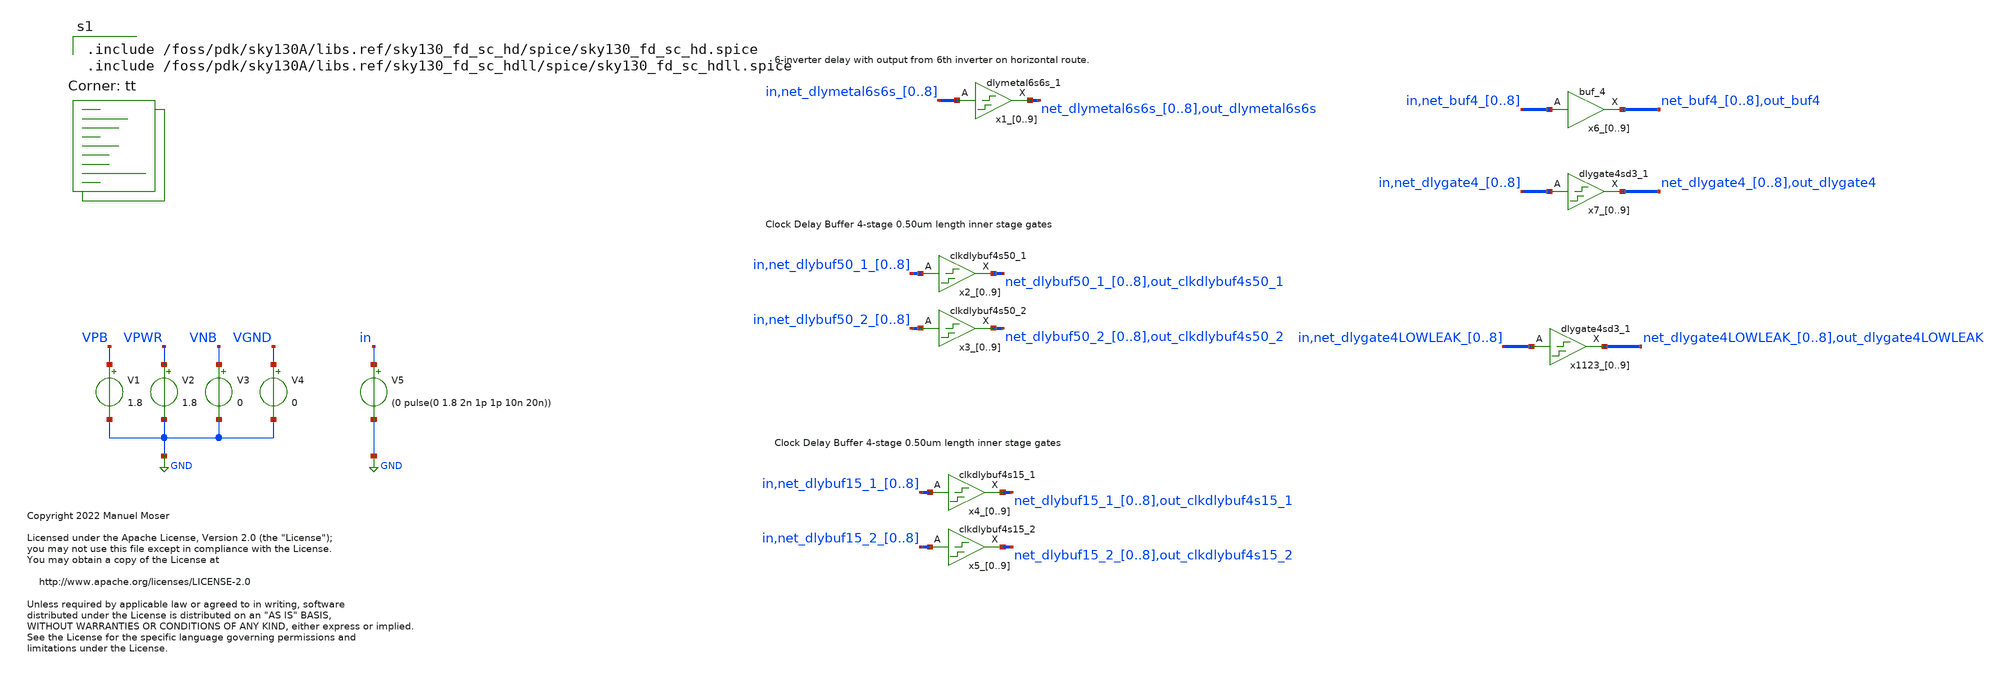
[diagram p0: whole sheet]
** sch_path: xschem/archive/adc_edge_detect_delay/delay_tb.sch
* Copyright 2022 Manuel Moser
* Licensed under the Apache License, Version 2.0 (the "License");
**.subckt delay_tb
x1_0 in VGND VNB VPB VPWR net_dlymetal6s6s_0 sky130_fd_sc_hd__dlymetal6s6s_1
x1_1 net_dlymetal6s6s_0 VGND VNB VPB VPWR net_dlymetal6s6s_1 sky130_fd_sc_hd__dlymetal6s6s_1
x1_2 net_dlymetal6s6s_1 VGND VNB VPB VPWR net_dlymetal6s6s_2 sky130_fd_sc_hd__dlymetal6s6s_1
x1_3 net_dlymetal6s6s_2 VGND VNB VPB VPWR net_dlymetal6s6s_3 sky130_fd_sc_hd__dlymetal6s6s_1
x1_4 net_dlymetal6s6s_3 VGND VNB VPB VPWR net_dlymetal6s6s_4 sky130_fd_sc_hd__dlymetal6s6s_1
x1_5 net_dlymetal6s6s_4 VGND VNB VPB VPWR net_dlymetal6s6s_5 sky130_fd_sc_hd__dlymetal6s6s_1
x1_6 net_dlymetal6s6s_5 VGND VNB VPB VPWR net_dlymetal6s6s_6 sky130_fd_sc_hd__dlymetal6s6s_1
x1_7 net_dlymetal6s6s_6 VGND VNB VPB VPWR net_dlymetal6s6s_7 sky130_fd_sc_hd__dlymetal6s6s_1
x1_8 net_dlymetal6s6s_7 VGND VNB VPB VPWR net_dlymetal6s6s_8 sky130_fd_sc_hd__dlymetal6s6s_1
x1_9 net_dlymetal6s6s_8 VGND VNB VPB VPWR out_dlymetal6s6s sky130_fd_sc_hd__dlymetal6s6s_1
x3_0 in VGND VNB VPB VPWR net_dlybuf50_2_0 sky130_fd_sc_hd__clkdlybuf4s50_2
x3_1 net_dlybuf50_2_0 VGND VNB VPB VPWR net_dlybuf50_2_1 sky130_fd_sc_hd__clkdlybuf4s50_2
x3_2 net_dlybuf50_2_1 VGND VNB VPB VPWR net_dlybuf50_2_2 sky130_fd_sc_hd__clkdlybuf4s50_2
x3_3 net_dlybuf50_2_2 VGND VNB VPB VPWR net_dlybuf50_2_3 sky130_fd_sc_hd__clkdlybuf4s50_2
x3_4 net_dlybuf50_2_3 VGND VNB VPB VPWR net_dlybuf50_2_4 sky130_fd_sc_hd__clkdlybuf4s50_2
x3_5 net_dlybuf50_2_4 VGND VNB VPB VPWR net_dlybuf50_2_5 sky130_fd_sc_hd__clkdlybuf4s50_2
x3_6 net_dlybuf50_2_5 VGND VNB VPB VPWR net_dlybuf50_2_6 sky130_fd_sc_hd__clkdlybuf4s50_2
x3_7 net_dlybuf50_2_6 VGND VNB VPB VPWR net_dlybuf50_2_7 sky130_fd_sc_hd__clkdlybuf4s50_2
x3_8 net_dlybuf50_2_7 VGND VNB VPB VPWR net_dlybuf50_2_8 sky130_fd_sc_hd__clkdlybuf4s50_2
x3_9 net_dlybuf50_2_8 VGND VNB VPB VPWR out_clkdlybuf4s50_2 sky130_fd_sc_hd__clkdlybuf4s50_2
x2_0 in VGND VNB VPB VPWR net_dlybuf50_1_0 sky130_fd_sc_hd__clkdlybuf4s50_1
x2_1 net_dlybuf50_1_0 VGND VNB VPB VPWR net_dlybuf50_1_1 sky130_fd_sc_hd__clkdlybuf4s50_1
x2_2 net_dlybuf50_1_1 VGND VNB VPB VPWR net_dlybuf50_1_2 sky130_fd_sc_hd__clkdlybuf4s50_1
x2_3 net_dlybuf50_1_2 VGND VNB VPB VPWR net_dlybuf50_1_3 sky130_fd_sc_hd__clkdlybuf4s50_1
x2_4 net_dlybuf50_1_3 VGND VNB VPB VPWR net_dlybuf50_1_4 sky130_fd_sc_hd__clkdlybuf4s50_1
x2_5 net_dlybuf50_1_4 VGND VNB VPB VPWR net_dlybuf50_1_5 sky130_fd_sc_hd__clkdlybuf4s50_1
x2_6 net_dlybuf50_1_5 VGND VNB VPB VPWR net_dlybuf50_1_6 sky130_fd_sc_hd__clkdlybuf4s50_1
x2_7 net_dlybuf50_1_6 VGND VNB VPB VPWR net_dlybuf50_1_7 sky130_fd_sc_hd__clkdlybuf4s50_1
x2_8 net_dlybuf50_1_7 VGND VNB VPB VPWR net_dlybuf50_1_8 sky130_fd_sc_hd__clkdlybuf4s50_1
x2_9 net_dlybuf50_1_8 VGND VNB VPB VPWR out_clkdlybuf4s50_1 sky130_fd_sc_hd__clkdlybuf4s50_1
V1 VPB GND 1.8
V2 VPWR GND 1.8
V3 VNB GND 0
V4 VGND GND 0
V5 in GND (0 pulse(0 1.8 2n 1p 1p 10n 20n))
x5_0 in VGND VNB VPB VPWR net_dlybuf15_2_0 sky130_fd_sc_hd__clkdlybuf4s15_2
x5_1 net_dlybuf15_2_0 VGND VNB VPB VPWR net_dlybuf15_2_1 sky130_fd_sc_hd__clkdlybuf4s15_2
x5_2 net_dlybuf15_2_1 VGND VNB VPB VPWR net_dlybuf15_2_2 sky130_fd_sc_hd__clkdlybuf4s15_2
x5_3 net_dlybuf15_2_2 VGND VNB VPB VPWR net_dlybuf15_2_3 sky130_fd_sc_hd__clkdlybuf4s15_2
x5_4 net_dlybuf15_2_3 VGND VNB VPB VPWR net_dlybuf15_2_4 sky130_fd_sc_hd__clkdlybuf4s15_2
x5_5 net_dlybuf15_2_4 VGND VNB VPB VPWR net_dlybuf15_2_5 sky130_fd_sc_hd__clkdlybuf4s15_2
x5_6 net_dlybuf15_2_5 VGND VNB VPB VPWR net_dlybuf15_2_6 sky130_fd_sc_hd__clkdlybuf4s15_2
x5_7 net_dlybuf15_2_6 VGND VNB VPB VPWR net_dlybuf15_2_7 sky130_fd_sc_hd__clkdlybuf4s15_2
x5_8 net_dlybuf15_2_7 VGND VNB VPB VPWR net_dlybuf15_2_8 sky130_fd_sc_hd__clkdlybuf4s15_2
x5_9 net_dlybuf15_2_8 VGND VNB VPB VPWR out_clkdlybuf4s15_2 sky130_fd_sc_hd__clkdlybuf4s15_2
x4_0 in VGND VNB VPB VPWR net_dlybuf15_1_0 sky130_fd_sc_hd__clkdlybuf4s15_1
x4_1 net_dlybuf15_1_0 VGND VNB VPB VPWR net_dlybuf15_1_1 sky130_fd_sc_hd__clkdlybuf4s15_1
x4_2 net_dlybuf15_1_1 VGND VNB VPB VPWR net_dlybuf15_1_2 sky130_fd_sc_hd__clkdlybuf4s15_1
x4_3 net_dlybuf15_1_2 VGND VNB VPB VPWR net_dlybuf15_1_3 sky130_fd_sc_hd__clkdlybuf4s15_1
x4_4 net_dlybuf15_1_3 VGND VNB VPB VPWR net_dlybuf15_1_4 sky130_fd_sc_hd__clkdlybuf4s15_1
x4_5 net_dlybuf15_1_4 VGND VNB VPB VPWR net_dlybuf15_1_5 sky130_fd_sc_hd__clkdlybuf4s15_1
x4_6 net_dlybuf15_1_5 VGND VNB VPB VPWR net_dlybuf15_1_6 sky130_fd_sc_hd__clkdlybuf4s15_1
x4_7 net_dlybuf15_1_6 VGND VNB VPB VPWR net_dlybuf15_1_7 sky130_fd_sc_hd__clkdlybuf4s15_1
x4_8 net_dlybuf15_1_7 VGND VNB VPB VPWR net_dlybuf15_1_8 sky130_fd_sc_hd__clkdlybuf4s15_1
x4_9 net_dlybuf15_1_8 VGND VNB VPB VPWR out_clkdlybuf4s15_1 sky130_fd_sc_hd__clkdlybuf4s15_1
x6_0 in VGND VNB VPB VPWR net_buf4_0 sky130_fd_sc_hd__buf_4
x6_1 net_buf4_0 VGND VNB VPB VPWR net_buf4_1 sky130_fd_sc_hd__buf_4
x6_2 net_buf4_1 VGND VNB VPB VPWR net_buf4_2 sky130_fd_sc_hd__buf_4
x6_3 net_buf4_2 VGND VNB VPB VPWR net_buf4_3 sky130_fd_sc_hd__buf_4
x6_4 net_buf4_3 VGND VNB VPB VPWR net_buf4_4 sky130_fd_sc_hd__buf_4
x6_5 net_buf4_4 VGND VNB VPB VPWR net_buf4_5 sky130_fd_sc_hd__buf_4
x6_6 net_buf4_5 VGND VNB VPB VPWR net_buf4_6 sky130_fd_sc_hd__buf_4
x6_7 net_buf4_6 VGND VNB VPB VPWR net_buf4_7 sky130_fd_sc_hd__buf_4
x6_8 net_buf4_7 VGND VNB VPB VPWR net_buf4_8 sky130_fd_sc_hd__buf_4
x6_9 net_buf4_8 VGND VNB VPB VPWR out_buf4 sky130_fd_sc_hd__buf_4
x7_0 in VGND VNB VPB VPWR net_dlygate4_0 sky130_fd_sc_hd__dlygate4sd3_1
x7_1 net_dlygate4_0 VGND VNB VPB VPWR net_dlygate4_1 sky130_fd_sc_hd__dlygate4sd3_1
x7_2 net_dlygate4_1 VGND VNB VPB VPWR net_dlygate4_2 sky130_fd_sc_hd__dlygate4sd3_1
x7_3 net_dlygate4_2 VGND VNB VPB VPWR net_dlygate4_3 sky130_fd_sc_hd__dlygate4sd3_1
x7_4 net_dlygate4_3 VGND VNB VPB VPWR net_dlygate4_4 sky130_fd_sc_hd__dlygate4sd3_1
x7_5 net_dlygate4_4 VGND VNB VPB VPWR net_dlygate4_5 sky130_fd_sc_hd__dlygate4sd3_1
x7_6 net_dlygate4_5 VGND VNB VPB VPWR net_dlygate4_6 sky130_fd_sc_hd__dlygate4sd3_1
x7_7 net_dlygate4_6 VGND VNB VPB VPWR net_dlygate4_7 sky130_fd_sc_hd__dlygate4sd3_1
x7_8 net_dlygate4_7 VGND VNB VPB VPWR net_dlygate4_8 sky130_fd_sc_hd__dlygate4sd3_1
x7_9 net_dlygate4_8 VGND VNB VPB VPWR out_dlygate4 sky130_fd_sc_hd__dlygate4sd3_1
x1123_0 in VGND VNB VPB VPWR net_dlygate4LOWLEAK_0 sky130_fd_sc_hdll__dlygate4sd3_1
x1123_1 net_dlygate4LOWLEAK_0 VGND VNB VPB VPWR net_dlygate4LOWLEAK_1
+ sky130_fd_sc_hdll__dlygate4sd3_1
x1123_2 net_dlygate4LOWLEAK_1 VGND VNB VPB VPWR net_dlygate4LOWLEAK_2
+ sky130_fd_sc_hdll__dlygate4sd3_1
x1123_3 net_dlygate4LOWLEAK_2 VGND VNB VPB VPWR net_dlygate4LOWLEAK_3
+ sky130_fd_sc_hdll__dlygate4sd3_1
x1123_4 net_dlygate4LOWLEAK_3 VGND VNB VPB VPWR net_dlygate4LOWLEAK_4
+ sky130_fd_sc_hdll__dlygate4sd3_1
x1123_5 net_dlygate4LOWLEAK_4 VGND VNB VPB VPWR net_dlygate4LOWLEAK_5
+ sky130_fd_sc_hdll__dlygate4sd3_1
x1123_6 net_dlygate4LOWLEAK_5 VGND VNB VPB VPWR net_dlygate4LOWLEAK_6
+ sky130_fd_sc_hdll__dlygate4sd3_1
x1123_7 net_dlygate4LOWLEAK_6 VGND VNB VPB VPWR net_dlygate4LOWLEAK_7
+ sky130_fd_sc_hdll__dlygate4sd3_1
x1123_8 net_dlygate4LOWLEAK_7 VGND VNB VPB VPWR net_dlygate4LOWLEAK_8
+ sky130_fd_sc_hdll__dlygate4sd3_1
x1123_9 net_dlygate4LOWLEAK_8 VGND VNB VPB VPWR out_dlygate4LOWLEAK sky130_fd_sc_hdll__dlygate4sd3_1
**** begin user architecture code

.save all
*.OPTIONS RELTOL=.001 TRTOL=1 ABSTOL=1e-16 CHGTOL=1.0e-16 DEFAD=1.0e-16

*uncomment for OP
*.op

.tran 1n 30n

*uncomment for TRANSIENT
.control
run
plot v(in) v(out_dlymetal6s6s) v(out_clkdlybuf4s50_1) v(out_clkdlybuf4s50_2) v(out_clkdlybuf4s15_1)
+ v(out_buf4) v(out_dlygate4) v(out_clkdlybuf4s15_2) v(out_dlygate4LOWLEAK)
.endc


.lib $::SKYWATER_MODELS/sky130.lib.spice tt

.include /foss/pdk/sky130A/libs.ref/sky130_fd_sc_hd/spice/sky130_fd_sc_hd.spice
.include /foss/pdk/sky130A/libs.ref/sky130_fd_sc_hdll/spice/sky130_fd_sc_hdll.spice

**** end user architecture code
**.ends
.GLOBAL GND
.end
